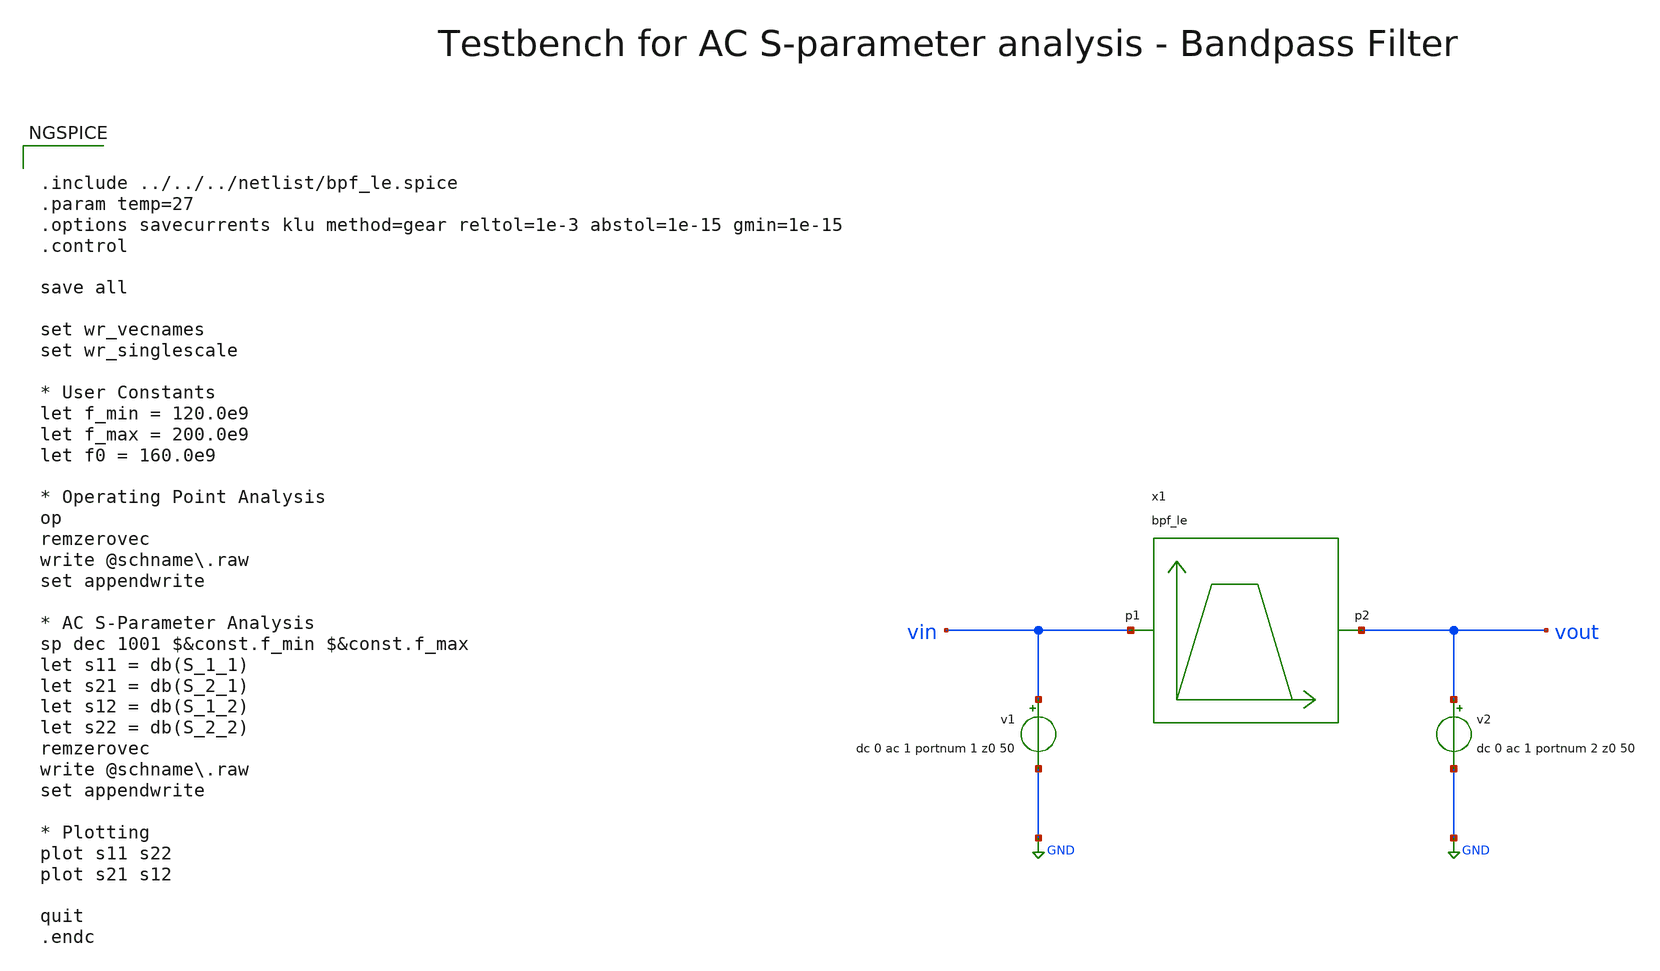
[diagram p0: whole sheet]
** sch_path: testbenches/xschem/bpf_le_tb_acsp.sch
**.subckt bpf_le_tb_acsp
v1 vin GND dc 0 ac 1 portnum 1 z0 50
v2 vout GND dc 0 ac 1 portnum 2 z0 50
x1 vin vout bpf_le
**** begin user architecture code


.include ../../../netlist/bpf_le.spice
.param temp=27
.options savecurrents klu method=gear reltol=1e-3 abstol=1e-15 gmin=1e-15
.control

save all

set wr_vecnames
set wr_singlescale

* User Constants
let f_min = 120.0e9
let f_max = 200.0e9
let f0 = 160.0e9

* Operating Point Analysis
op
remzerovec
write @schname\.raw
set appendwrite

* AC S-Parameter Analysis
sp dec 1001 $&const.f_min $&const.f_max
let s11 = db(S_1_1)
let s21 = db(S_2_1)
let s12 = db(S_1_2)
let s22 = db(S_2_2)
remzerovec
write @schname\.raw
set appendwrite

* Plotting
plot s11 s22
plot s21 s12

quit
.endc



.lib cornerMOSlv.lib mos_tt
.lib cornerMOShv.lib mos_tt
.lib cornerHBT.lib hbt_typ
.lib cornerRES.lib res_typ
.lib cornerCAP.lib cap_typ
.lib cornerDIO.lib dio_tt

**** end user architecture code
**.ends
.GLOBAL GND
.end
